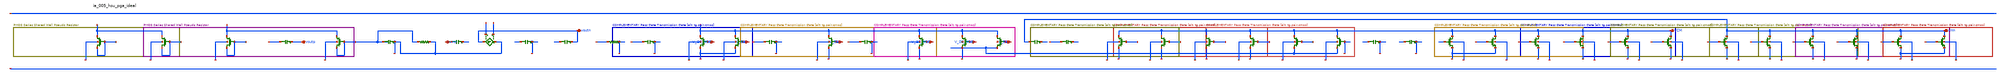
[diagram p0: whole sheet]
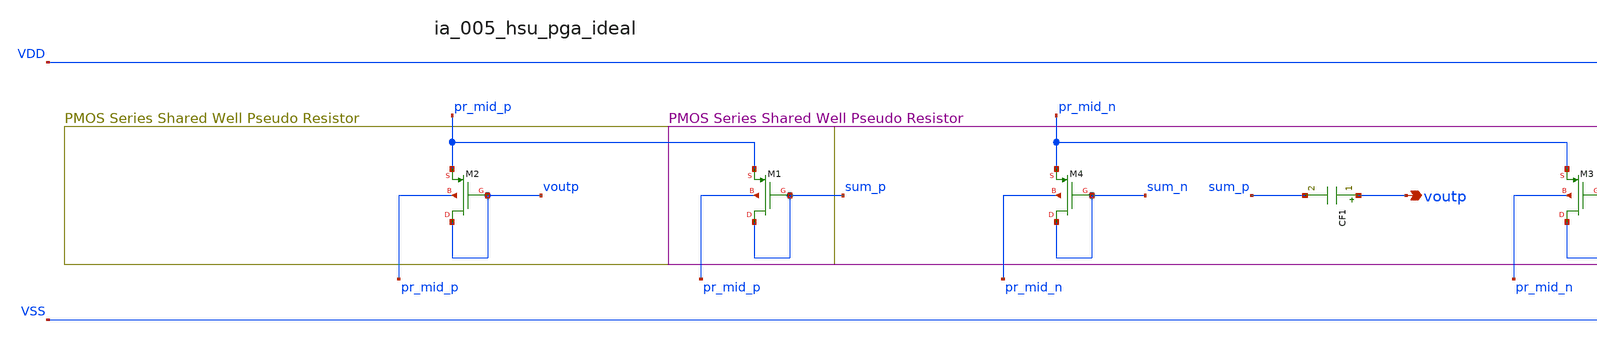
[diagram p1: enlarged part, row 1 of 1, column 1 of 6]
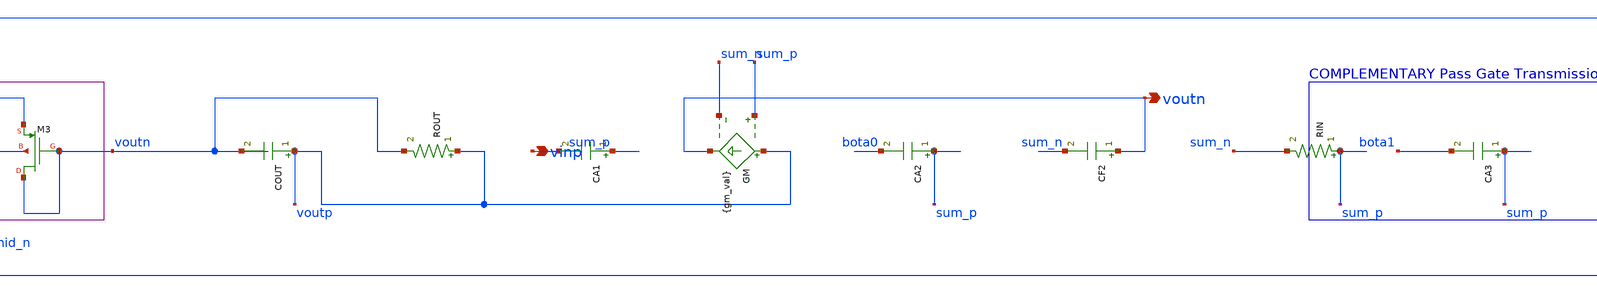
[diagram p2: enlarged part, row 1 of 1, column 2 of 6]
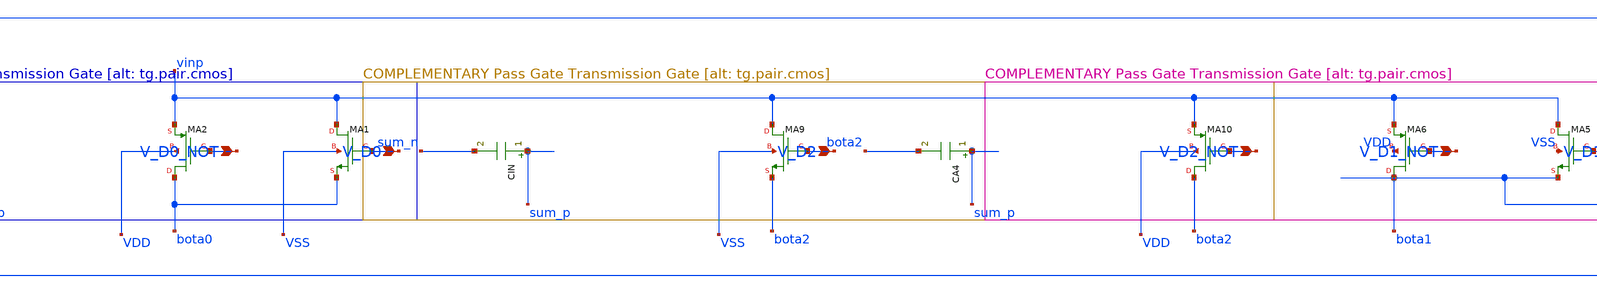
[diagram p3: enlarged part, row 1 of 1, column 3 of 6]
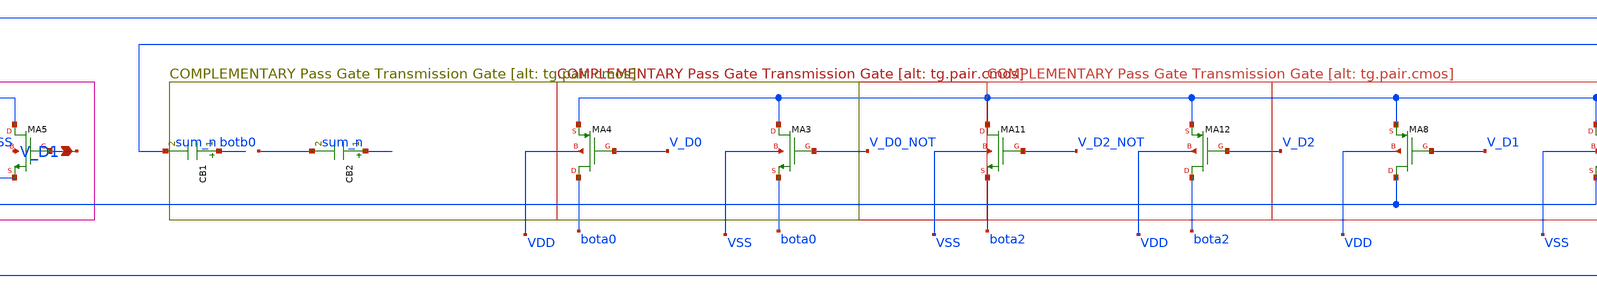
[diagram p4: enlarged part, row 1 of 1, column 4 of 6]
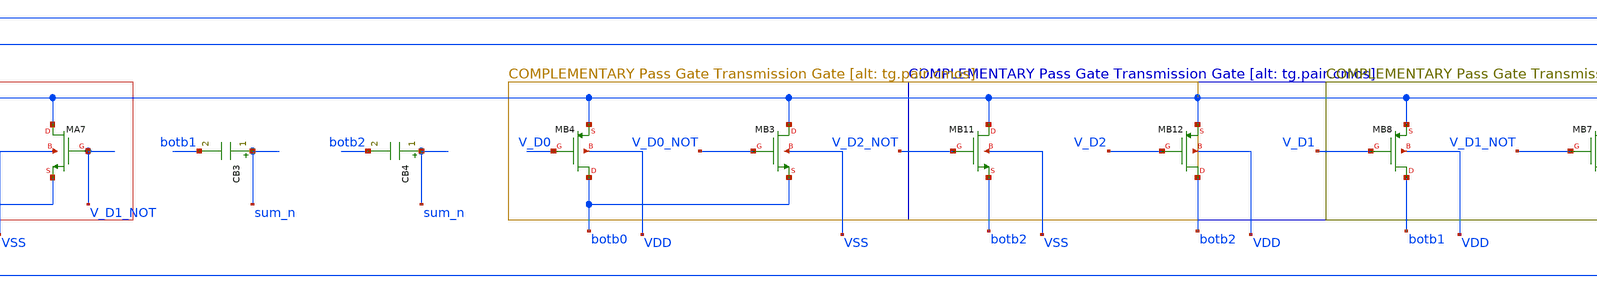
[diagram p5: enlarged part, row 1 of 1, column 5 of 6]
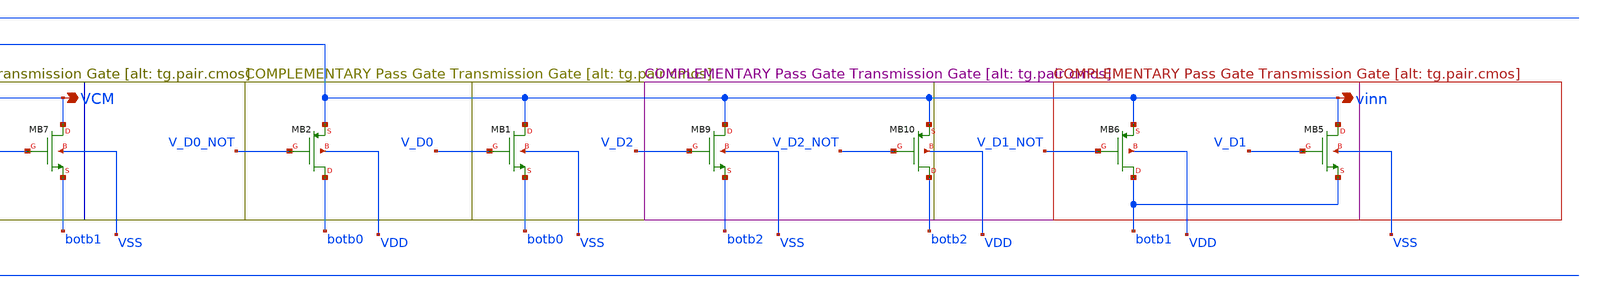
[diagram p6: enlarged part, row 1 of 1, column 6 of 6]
** sch_path: analog-db/raw/ia_005_hsu_pga_ideal/ia_005_hsu_pga_ideal_annotated.sch
**.subckt ia_005_hsu_pga_ideal_annotated V_D0_NOT V_D0 V_D2 V_D2_NOT V_D1_NOT V_D1 vinp VCM vinn
*+ voutp voutn
*.ipin V_D0_NOT
*.ipin V_D0
*.ipin V_D2
*.ipin V_D2_NOT
*.ipin V_D1_NOT
*.ipin V_D1
*.opin vinp
*.opin VCM
*.opin vinn
*.opin voutp
*.opin voutn
CA1 sum_p vinp 'Cu' m=x_dut_ca1_m
CA2 sum_p bota0 'Cu' m=x_dut_ca2_m
CA3 sum_p bota1 'Cu' m=x_dut_ca3_m
CA4 sum_p bota2 'Cu' m=x_dut_ca4_m
CB1 sum_n vinn 'Cu' m=x_dut_cb1_m
CB2 sum_n botb0 'Cu' m=x_dut_cb2_m
CB3 sum_n botb1 'Cu' m=x_dut_cb3_m
CB4 sum_n botb2 'Cu' m=x_dut_cb4_m
CF1 voutp sum_p 'x_dut_cf1_value' m=1
CF2 voutn sum_n 'x_dut_cf2_value' m=1
CIN sum_p sum_n 'cin_val' m=1
COUT voutp voutn 'cout_val' m=1
GM voutp voutn sum_p sum_n {gm_val}
RIN sum_p sum_n 'rin_val' m=1
ROUT voutp voutn 'rout_val' m=1
XM1 sum_p sum_p pr_mid_p pr_mid_p sg13_lv_pmos w=x_dut_xm1_w l=x_dut_xm1_l ng=1 m=x_dut_xm1_m
XM2 voutp voutp pr_mid_p pr_mid_p sg13_lv_pmos w=x_dut_xm2_w l=x_dut_xm2_l ng=1 m=x_dut_xm2_m
XM3 voutn voutn pr_mid_n pr_mid_n sg13_lv_pmos w=x_dut_xm3_w l=x_dut_xm3_l ng=1 m=x_dut_xm3_m
XM4 sum_n sum_n pr_mid_n pr_mid_n sg13_lv_pmos w=x_dut_xm4_w l=x_dut_xm4_l ng=1 m=x_dut_xm4_m
XMA1 vinp V_D0 bota0 VSS sg13_lv_nmos w=x_dut_xma1_w l=x_dut_xma1_l ng=1 m=x_dut_xma1_m
XMA10 bota2 V_D2_NOT vinp VDD sg13_lv_pmos w=x_dut_xma10_w l=x_dut_xma10_l ng=1 m=x_dut_xma10_m
XMA11 VCM V_D2_NOT bota2 VSS sg13_lv_nmos w=x_dut_xma11_w l=x_dut_xma11_l ng=1 m=x_dut_xma11_m
XMA12 bota2 V_D2 VCM VDD sg13_lv_pmos w=x_dut_xma12_w l=x_dut_xma12_l ng=1 m=x_dut_xma12_m
XMA2 bota0 V_D0_NOT vinp VDD sg13_lv_pmos w=x_dut_xma2_w l=x_dut_xma2_l ng=1 m=x_dut_xma2_m
XMA3 VCM V_D0_NOT bota0 VSS sg13_lv_nmos w=x_dut_xma3_w l=x_dut_xma3_l ng=1 m=x_dut_xma3_m
XMA4 bota0 V_D0 VCM VDD sg13_lv_pmos w=x_dut_xma4_w l=x_dut_xma4_l ng=1 m=x_dut_xma4_m
XMA5 vinp V_D1 bota1 VSS sg13_lv_nmos w=x_dut_xma5_w l=x_dut_xma5_l ng=1 m=x_dut_xma5_m
XMA6 bota1 V_D1_NOT vinp VDD sg13_lv_pmos w=x_dut_xma6_w l=x_dut_xma6_l ng=1 m=x_dut_xma6_m
XMA7 VCM V_D1_NOT bota1 VSS sg13_lv_nmos w=x_dut_xma7_w l=x_dut_xma7_l ng=1 m=x_dut_xma7_m
XMA8 bota1 V_D1 VCM VDD sg13_lv_pmos w=x_dut_xma8_w l=x_dut_xma8_l ng=1 m=x_dut_xma8_m
XMA9 vinp V_D2 bota2 VSS sg13_lv_nmos w=x_dut_xma9_w l=x_dut_xma9_l ng=1 m=x_dut_xma9_m
XMB1 vinn V_D0 botb0 VSS sg13_lv_nmos w=x_dut_xmb1_w l=x_dut_xmb1_l ng=1 m=x_dut_xmb1_m
XMB10 botb2 V_D2_NOT vinn VDD sg13_lv_pmos w=x_dut_xmb10_w l=x_dut_xmb10_l ng=1 m=x_dut_xmb10_m
XMB11 VCM V_D2_NOT botb2 VSS sg13_lv_nmos w=x_dut_xmb11_w l=x_dut_xmb11_l ng=1 m=x_dut_xmb11_m
XMB12 botb2 V_D2 VCM VDD sg13_lv_pmos w=x_dut_xmb12_w l=x_dut_xmb12_l ng=1 m=x_dut_xmb12_m
XMB2 botb0 V_D0_NOT vinn VDD sg13_lv_pmos w=x_dut_xmb2_w l=x_dut_xmb2_l ng=1 m=x_dut_xmb2_m
XMB3 VCM V_D0_NOT botb0 VSS sg13_lv_nmos w=x_dut_xmb3_w l=x_dut_xmb3_l ng=1 m=x_dut_xmb3_m
XMB4 botb0 V_D0 VCM VDD sg13_lv_pmos w=x_dut_xmb4_w l=x_dut_xmb4_l ng=1 m=x_dut_xmb4_m
XMB5 vinn V_D1 botb1 VSS sg13_lv_nmos w=x_dut_xmb5_w l=x_dut_xmb5_l ng=1 m=x_dut_xmb5_m
XMB6 botb1 V_D1_NOT vinn VDD sg13_lv_pmos w=x_dut_xmb6_w l=x_dut_xmb6_l ng=1 m=x_dut_xmb6_m
XMB7 VCM V_D1_NOT botb1 VSS sg13_lv_nmos w=x_dut_xmb7_w l=x_dut_xmb7_l ng=1 m=x_dut_xmb7_m
XMB8 botb1 V_D1 VCM VDD sg13_lv_pmos w=x_dut_xmb8_w l=x_dut_xmb8_l ng=1 m=x_dut_xmb8_m
XMB9 vinn V_D2 botb2 VSS sg13_lv_nmos w=x_dut_xmb9_w l=x_dut_xmb9_l ng=1 m=x_dut_xmb9_m
**.ends
.end
